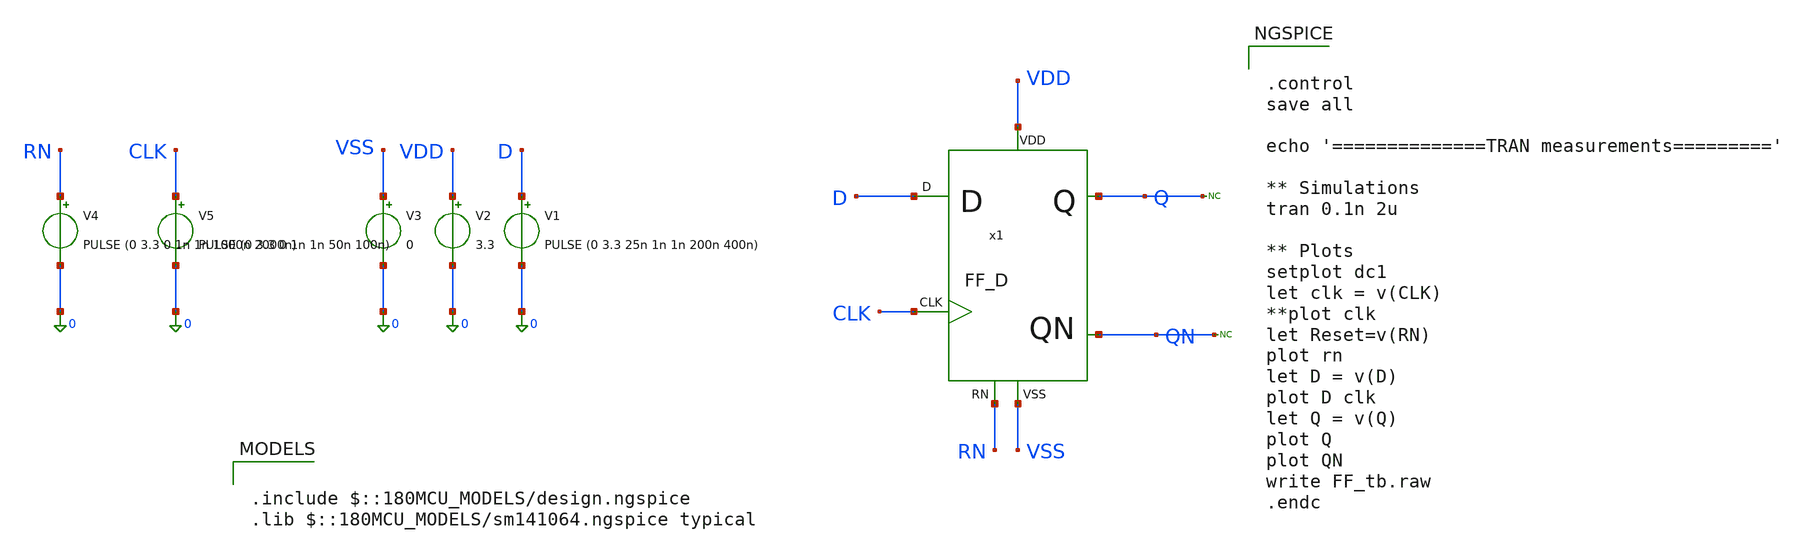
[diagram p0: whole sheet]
** sch_path: designs/sar_adc/digital/flip_flop/xschem/FF_tb.sch
**.subckt FF_tb
V1 D 0 PULSE (0 3.3 25n 1n 1n 200n 400n)
V2 VDD 0 3.3
V3 VSS 0 0
V5 CLK 0 PULSE (0 3.3 0 1n 1n 50n 100n)
x1 CLK D VDD VSS Q RN QN FF_D
V4 RN 0 PULSE (0 3.3 0 1n 1n 1000n 2000n)
* noconn Q
* noconn QN
**** begin user architecture code

.include $::180MCU_MODELS/design.ngspice
.lib $::180MCU_MODELS/sm141064.ngspice typical



.control
save all

echo '==============TRAN measurements========='

** Simulations
tran 0.1n 2u

** Plots
setplot dc1
let clk = v(CLK)
**plot clk
let Reset=v(RN)
plot rn
let D = v(D)
plot D clk
let Q = v(Q)
plot Q
plot QN
write FF_tb.raw
.endc


**** end user architecture code
**.ends
.end
